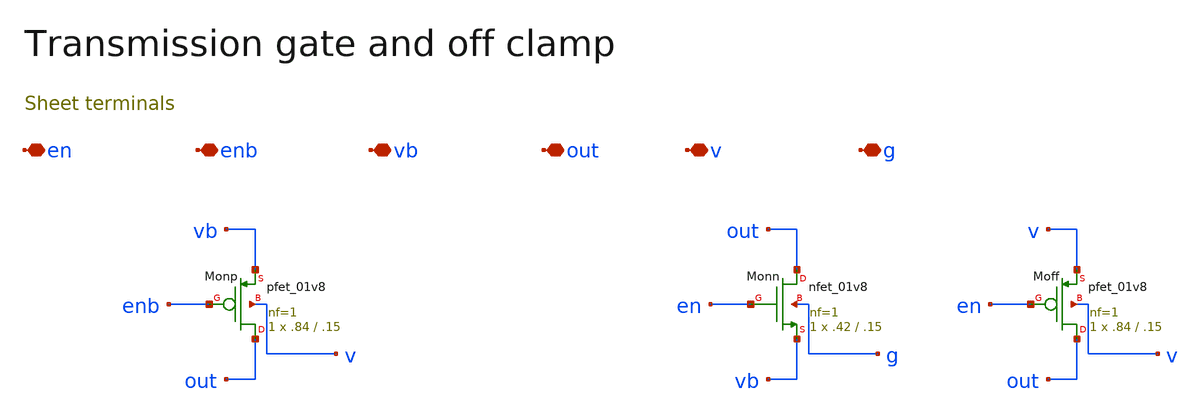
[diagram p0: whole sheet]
** sch_path: review/xschem/tailgate.sch
**.subckt tailgate en enb vb out v g
*.iopin en
*.iopin enb
*.iopin vb
*.iopin out
*.iopin v
*.iopin g
XMonp out enb vb v sky130_fd_pr__pfet_01v8 L=.15 W=.84 nf=1 ad='int((nf+1)/2) * W/nf * 0.29' as='int((nf+2)/2) * W/nf * 0.29'
+ pd='2*int((nf+1)/2) * (W/nf + 0.29)' ps='2*int((nf+2)/2) * (W/nf + 0.29)' nrd='0.29 / W' nrs='0.29 / W'
+ sa=0 sb=0 sd=0 mult=1 m=1
XMonn out en vb g sky130_fd_pr__nfet_01v8 L=.15 W=.42 nf=1 ad='int((1 + 1)/2) * .42 / 1 * 0.29' as='int((1 + 2)/2) * .42 / 1 * 0.29'
+ pd='2*int((1 + 1)/2) * (.42 / 1 + 0.29)' ps='2*int((1 + 2)/2) * (.42 / 1 + 0.29)' nrd='0.29 / .42 ' nrs='0.29 / .42 '
+ sa=0 sb=0 sd=0 mult=1 m=1
XMoff out en v v sky130_fd_pr__pfet_01v8 L=.15 W=.84 nf=1 ad='int((nf+1)/2) * W/nf * 0.29' as='int((nf+2)/2) * W/nf * 0.29'
+ pd='2*int((nf+1)/2) * (W/nf + 0.29)' ps='2*int((nf+2)/2) * (W/nf + 0.29)' nrd='0.29 / W' nrs='0.29 / W'
+ sa=0 sb=0 sd=0 mult=1 m=1
**.ends
.end
